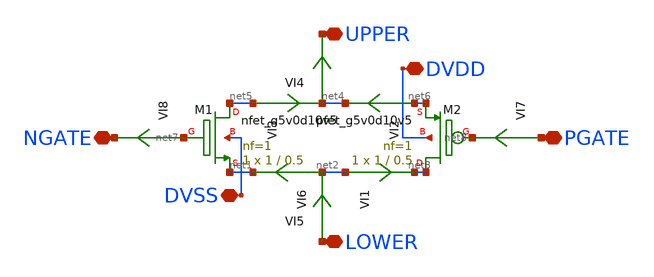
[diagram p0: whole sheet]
** sch_path: xschem/T_Gate_5V.sch
**.subckt T_Gate_5V PGATE UPPER LOWER NGATE DVDD DVSS
*.iopin PGATE
*.iopin UPPER
*.iopin LOWER
*.iopin NGATE
*.iopin DVDD
*.iopin DVSS
VI6 net2 net1 0
.save i(vi6)
VI1 net2 net3 0
.save i(vi1)
VI2 net6 net4 0
.save i(vi2)
VI3 net5 net4 0
.save i(vi3)
XM1 net5 net7 net1 DVSS sky130_fd_pr__nfet_g5v0d10v5 L=0.5 W=1 nf=1 ad='int((nf+1)/2) * W/nf * 0.29'
+ as='int((nf+2)/2) * W/nf * 0.29' pd='2*int((nf+1)/2) * (W/nf + 0.29)' ps='2*int((nf+2)/2) * (W/nf + 0.29)'
+ nrd='0.29 / W' nrs='0.29 / W' sa=0 sb=0 sd=0 mult=1 m=1
XM2 net3 net8 net6 DVDD sky130_fd_pr__pfet_g5v0d10v5 L=0.5 W=1 nf=1 ad='int((nf+1)/2) * W/nf * 0.29'
+ as='int((nf+2)/2) * W/nf * 0.29' pd='2*int((nf+1)/2) * (W/nf + 0.29)' ps='2*int((nf+2)/2) * (W/nf + 0.29)'
+ nrd='0.29 / W' nrs='0.29 / W' sa=0 sb=0 sd=0 mult=1 m=1
VI4 net4 UPPER 0
.save i(vi4)
VI5 LOWER net2 0
.save i(vi5)
VI7 PGATE net8 0
.save i(vi7)
VI8 net7 NGATE 0
.save i(vi8)
**.ends
.end
